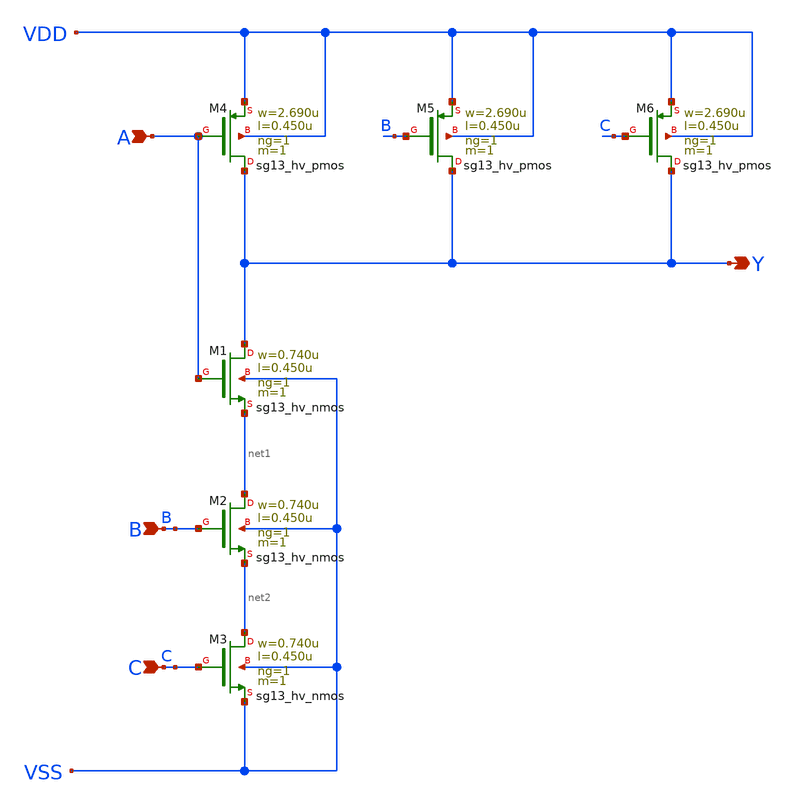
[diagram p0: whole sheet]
** sch_path: ihp-sg13g2/libs.ref/sg13g2_stdcell_hv/sch/xschem/sg13g2_hv_nand3_1.sch
* Copyright 2023 IHP PDK Authors
* Licensed under the Apache License, Version 2.0 (the "License");
* you may not use this file except in compliance with the License.
* You may obtain a copy of the License at
* https://www.apache.org/licenses/LICENSE-2.0
* Unless required by applicable law or agreed to in writing, software
* distributed under the License is distributed on an "AS IS" BASIS,
* WITHOUT WARRANTIES OR CONDITIONS OF ANY KIND, either express or implied.
* See the License for the specific language governing permissions and
* limitations under the License.
**.subckt sg13g2_hv_nand3_1 A B C Y
*.ipin A
*.ipin B
*.ipin C
*.opin Y
XM1 Y A net1 VSS sg13_hv_nmos w=0.740u l=0.450u ng=1 m=1 mm_ok=1
XM2 net1 B net2 VSS sg13_hv_nmos w=0.740u l=0.450u ng=1 m=1 mm_ok=1
XM3 net2 C VSS VSS sg13_hv_nmos w=0.740u l=0.450u ng=1 m=1 mm_ok=1
XM4 Y A VDD VDD sg13_hv_pmos w=2.690u l=0.450u ng=1 m=1 mm_ok=1
XM5 Y B VDD VDD sg13_hv_pmos w=2.690u l=0.450u ng=1 m=1 mm_ok=1
XM6 Y C VDD VDD sg13_hv_pmos w=2.690u l=0.450u ng=1 m=1 mm_ok=1
**.ends
.end
